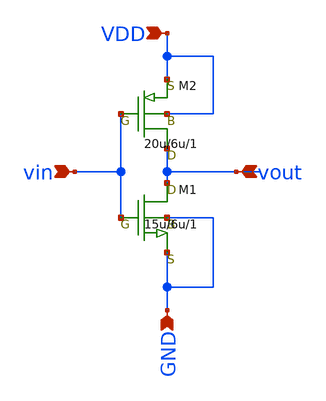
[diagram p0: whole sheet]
** sch_path: Submitted/inverter_radioheadozawa.sch
**.subckt inverter_radioheadozawa VDD vin vout GND
*.ipin VDD
*.ipin vin
*.ipin vout
*.ipin GND
M1 vout vin GND GND nch w=15u l=6u as=0 ps=0 ad=0 pd=0 m=1
M2 vout vin VDD VDD pch w=20u l=6u as=0 ps=0 ad=0 pd=0 m=1
**.ends
.end
